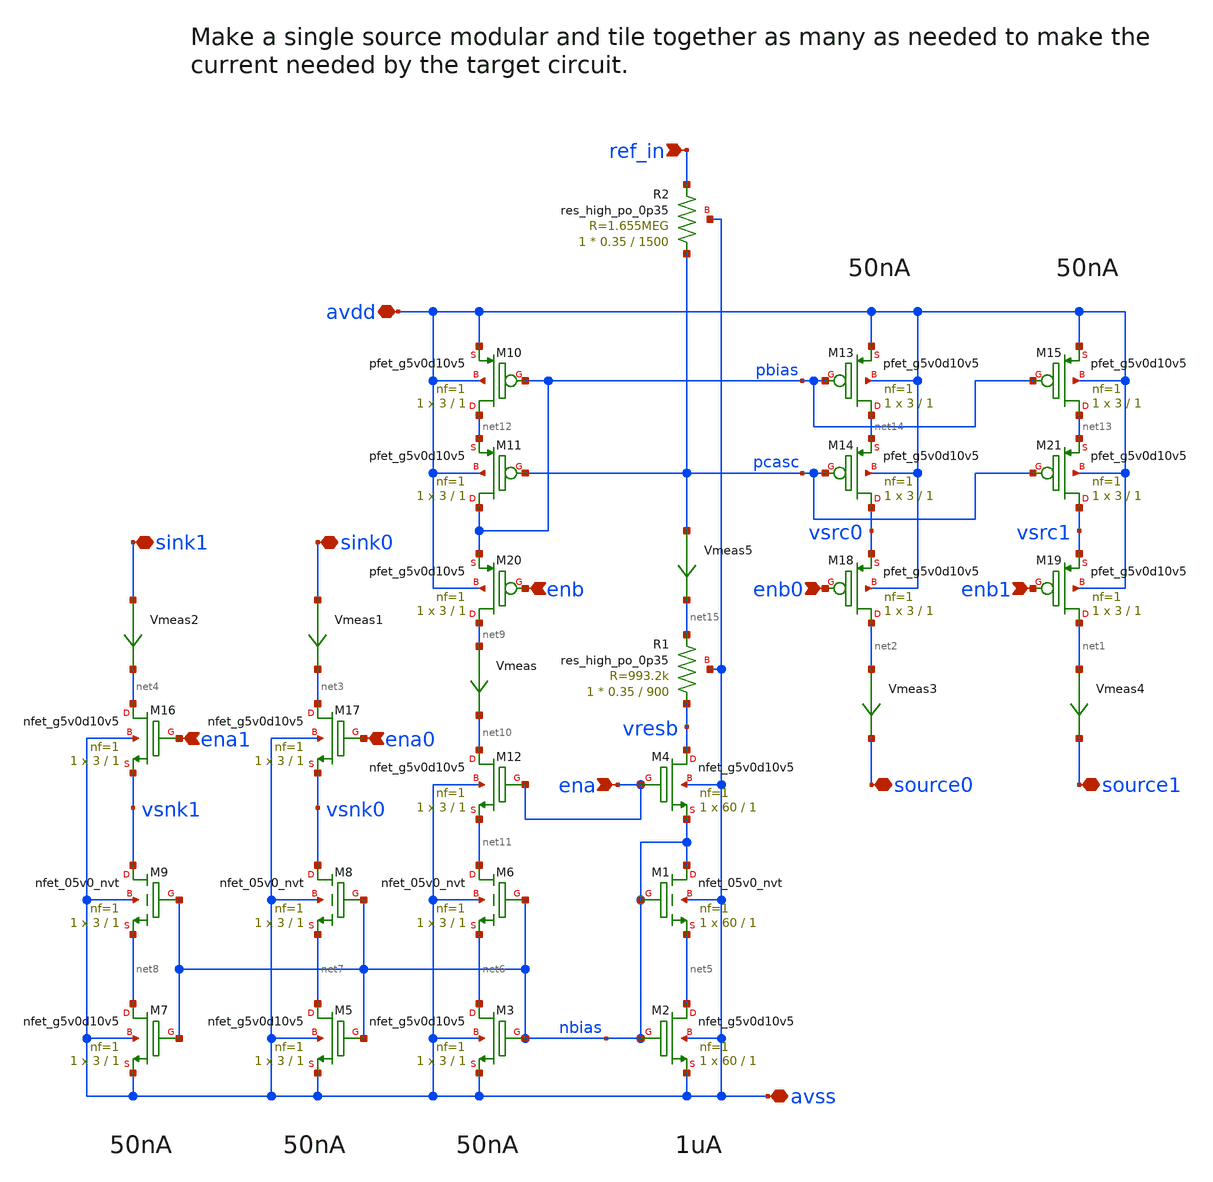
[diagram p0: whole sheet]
** sch_path: xschem/bias_generator_test.sch
**.subckt bias_generator_test ref_in sink0 sink1 avss ena avdd source1 source0 ena0 ena1 enb enb0
*+ enb1
*.ipin ref_in
*.iopin sink0
*.iopin sink1
*.iopin avss
*.ipin ena
*.iopin avdd
*.iopin source1
*.iopin source0
*.ipin ena0
*.ipin ena1
*.ipin enb
*.ipin enb0
*.ipin enb1
XR1 vresb net15 avss sky130_fd_pr__res_high_po_0p35 L=900 mult=1 m=1
XM2 net5 nbias avss avss sky130_fd_pr__nfet_g5v0d10v5 L=1 W=60 nf=1 ad='int((nf+1)/2) * W/nf * 0.29'
+ as='int((nf+2)/2) * W/nf * 0.29' pd='2*int((nf+1)/2) * (W/nf + 0.29)' ps='2*int((nf+2)/2) * (W/nf + 0.29)'
+ nrd='0.29 / W' nrs='0.29 / W' sa=0 sb=0 sd=0 mult=1 m=1
XM3 net6 nbias avss avss sky130_fd_pr__nfet_g5v0d10v5 L=1 W=3 nf=1 ad='int((nf+1)/2) * W/nf * 0.29' as='int((nf+2)/2) * W/nf * 0.29'
+ pd='2*int((nf+1)/2) * (W/nf + 0.29)' ps='2*int((nf+2)/2) * (W/nf + 0.29)' nrd='0.29 / W' nrs='0.29 / W'
+ sa=0 sb=0 sd=0 mult=1 m=1
XM5 net7 nbias avss avss sky130_fd_pr__nfet_g5v0d10v5 L=1 W=3 nf=1 ad='int((nf+1)/2) * W/nf * 0.29' as='int((nf+2)/2) * W/nf * 0.29'
+ pd='2*int((nf+1)/2) * (W/nf + 0.29)' ps='2*int((nf+2)/2) * (W/nf + 0.29)' nrd='0.29 / W' nrs='0.29 / W'
+ sa=0 sb=0 sd=0 mult=1 m=1
XM7 net8 nbias avss avss sky130_fd_pr__nfet_g5v0d10v5 L=1 W=3 nf=1 ad='int((nf+1)/2) * W/nf * 0.29' as='int((nf+2)/2) * W/nf * 0.29'
+ pd='2*int((nf+1)/2) * (W/nf + 0.29)' ps='2*int((nf+2)/2) * (W/nf + 0.29)' nrd='0.29 / W' nrs='0.29 / W'
+ sa=0 sb=0 sd=0 mult=1 m=1
XM10 net12 pbias avdd avdd sky130_fd_pr__pfet_g5v0d10v5 L=1 W=3 nf=1 ad='int((nf+1)/2) * W/nf * 0.29'
+ as='int((nf+2)/2) * W/nf * 0.29' pd='2*int((nf+1)/2) * (W/nf + 0.29)' ps='2*int((nf+2)/2) * (W/nf + 0.29)'
+ nrd='0.29 / W' nrs='0.29 / W' sa=0 sb=0 sd=0 mult=1 m=1
XM13 net14 pbias avdd avdd sky130_fd_pr__pfet_g5v0d10v5 L=1 W=3 nf=1 ad='int((nf+1)/2) * W/nf * 0.29'
+ as='int((nf+2)/2) * W/nf * 0.29' pd='2*int((nf+1)/2) * (W/nf + 0.29)' ps='2*int((nf+2)/2) * (W/nf + 0.29)'
+ nrd='0.29 / W' nrs='0.29 / W' sa=0 sb=0 sd=0 mult=1 m=1
XM15 net13 pbias avdd avdd sky130_fd_pr__pfet_g5v0d10v5 L=1 W=3 nf=1 ad='int((nf+1)/2) * W/nf * 0.29'
+ as='int((nf+2)/2) * W/nf * 0.29' pd='2*int((nf+1)/2) * (W/nf + 0.29)' ps='2*int((nf+2)/2) * (W/nf + 0.29)'
+ nrd='0.29 / W' nrs='0.29 / W' sa=0 sb=0 sd=0 mult=1 m=1
XM18 net2 enb0 vsrc0 avdd sky130_fd_pr__pfet_g5v0d10v5 L=1 W=3 nf=1 ad='int((nf+1)/2) * W/nf * 0.29'
+ as='int((nf+2)/2) * W/nf * 0.29' pd='2*int((nf+1)/2) * (W/nf + 0.29)' ps='2*int((nf+2)/2) * (W/nf + 0.29)'
+ nrd='0.29 / W' nrs='0.29 / W' sa=0 sb=0 sd=0 mult=1 m=1
XM19 net1 enb1 vsrc1 avdd sky130_fd_pr__pfet_g5v0d10v5 L=1 W=3 nf=1 ad='int((nf+1)/2) * W/nf * 0.29'
+ as='int((nf+2)/2) * W/nf * 0.29' pd='2*int((nf+1)/2) * (W/nf + 0.29)' ps='2*int((nf+2)/2) * (W/nf + 0.29)'
+ nrd='0.29 / W' nrs='0.29 / W' sa=0 sb=0 sd=0 mult=1 m=1
XM20 net9 enb pbias avdd sky130_fd_pr__pfet_g5v0d10v5 L=1 W=3 nf=1 ad='int((nf+1)/2) * W/nf * 0.29' as='int((nf+2)/2) * W/nf * 0.29'
+ pd='2*int((nf+1)/2) * (W/nf + 0.29)' ps='2*int((nf+2)/2) * (W/nf + 0.29)' nrd='0.29 / W' nrs='0.29 / W'
+ sa=0 sb=0 sd=0 mult=1 m=1
Vmeas net9 net10 0
.save i(vmeas)
Vmeas1 sink0 net3 0
.save i(vmeas1)
Vmeas2 sink1 net4 0
.save i(vmeas2)
Vmeas3 net2 source0 0
.save i(vmeas3)
Vmeas4 net1 source1 0
.save i(vmeas4)
Vmeas5 pcasc net15 0
.save i(vmeas5)
XM4 vresb ena nbias avss sky130_fd_pr__nfet_g5v0d10v5 L=1 W=60 nf=1 ad='int((nf+1)/2) * W/nf * 0.29'
+ as='int((nf+2)/2) * W/nf * 0.29' pd='2*int((nf+1)/2) * (W/nf + 0.29)' ps='2*int((nf+2)/2) * (W/nf + 0.29)'
+ nrd='0.29 / W' nrs='0.29 / W' sa=0 sb=0 sd=0 mult=1 m=1
XM16 net4 ena1 vsnk1 avss sky130_fd_pr__nfet_g5v0d10v5 L=1 W=3 nf=1 ad='int((nf+1)/2) * W/nf * 0.29'
+ as='int((nf+2)/2) * W/nf * 0.29' pd='2*int((nf+1)/2) * (W/nf + 0.29)' ps='2*int((nf+2)/2) * (W/nf + 0.29)'
+ nrd='0.29 / W' nrs='0.29 / W' sa=0 sb=0 sd=0 mult=1 m=1
XM17 net3 ena0 vsnk0 avss sky130_fd_pr__nfet_g5v0d10v5 L=1 W=3 nf=1 ad='int((nf+1)/2) * W/nf * 0.29'
+ as='int((nf+2)/2) * W/nf * 0.29' pd='2*int((nf+1)/2) * (W/nf + 0.29)' ps='2*int((nf+2)/2) * (W/nf + 0.29)'
+ nrd='0.29 / W' nrs='0.29 / W' sa=0 sb=0 sd=0 mult=1 m=1
XM1 nbias nbias net5 avss sky130_fd_pr__nfet_05v0_nvt L=1 W=60 nf=1 ad='int((nf+1)/2) * W/nf * 0.29'
+ as='int((nf+2)/2) * W/nf * 0.29' pd='2*int((nf+1)/2) * (W/nf + 0.29)' ps='2*int((nf+2)/2) * (W/nf + 0.29)'
+ nrd='0.29 / W' nrs='0.29 / W' sa=0 sb=0 sd=0 mult=1 m=1
XM6 net11 nbias net6 avss sky130_fd_pr__nfet_05v0_nvt L=1 W=3 nf=1 ad='int((nf+1)/2) * W/nf * 0.29' as='int((nf+2)/2) * W/nf * 0.29'
+ pd='2*int((nf+1)/2) * (W/nf + 0.29)' ps='2*int((nf+2)/2) * (W/nf + 0.29)' nrd='0.29 / W' nrs='0.29 / W'
+ sa=0 sb=0 sd=0 mult=1 m=1
XM8 vsnk0 nbias net7 avss sky130_fd_pr__nfet_05v0_nvt L=1 W=3 nf=1 ad='int((nf+1)/2) * W/nf * 0.29' as='int((nf+2)/2) * W/nf * 0.29'
+ pd='2*int((nf+1)/2) * (W/nf + 0.29)' ps='2*int((nf+2)/2) * (W/nf + 0.29)' nrd='0.29 / W' nrs='0.29 / W'
+ sa=0 sb=0 sd=0 mult=1 m=1
XM9 vsnk1 nbias net8 avss sky130_fd_pr__nfet_05v0_nvt L=1 W=3 nf=1 ad='int((nf+1)/2) * W/nf * 0.29' as='int((nf+2)/2) * W/nf * 0.29'
+ pd='2*int((nf+1)/2) * (W/nf + 0.29)' ps='2*int((nf+2)/2) * (W/nf + 0.29)' nrd='0.29 / W' nrs='0.29 / W'
+ sa=0 sb=0 sd=0 mult=1 m=1
XM12 net10 ena net11 avss sky130_fd_pr__nfet_g5v0d10v5 L=1 W=3 nf=1 ad='int((nf+1)/2) * W/nf * 0.29'
+ as='int((nf+2)/2) * W/nf * 0.29' pd='2*int((nf+1)/2) * (W/nf + 0.29)' ps='2*int((nf+2)/2) * (W/nf + 0.29)'
+ nrd='0.29 / W' nrs='0.29 / W' sa=0 sb=0 sd=0 mult=1 m=1
XM11 pbias pcasc net12 avdd sky130_fd_pr__pfet_g5v0d10v5 L=1 W=3 nf=1 ad='int((nf+1)/2) * W/nf * 0.29'
+ as='int((nf+2)/2) * W/nf * 0.29' pd='2*int((nf+1)/2) * (W/nf + 0.29)' ps='2*int((nf+2)/2) * (W/nf + 0.29)'
+ nrd='0.29 / W' nrs='0.29 / W' sa=0 sb=0 sd=0 mult=1 m=1
XM14 vsrc0 pcasc net14 avdd sky130_fd_pr__pfet_g5v0d10v5 L=1 W=3 nf=1 ad='int((nf+1)/2) * W/nf * 0.29'
+ as='int((nf+2)/2) * W/nf * 0.29' pd='2*int((nf+1)/2) * (W/nf + 0.29)' ps='2*int((nf+2)/2) * (W/nf + 0.29)'
+ nrd='0.29 / W' nrs='0.29 / W' sa=0 sb=0 sd=0 mult=1 m=1
XM21 vsrc1 pcasc net13 avdd sky130_fd_pr__pfet_g5v0d10v5 L=1 W=3 nf=1 ad='int((nf+1)/2) * W/nf * 0.29'
+ as='int((nf+2)/2) * W/nf * 0.29' pd='2*int((nf+1)/2) * (W/nf + 0.29)' ps='2*int((nf+2)/2) * (W/nf + 0.29)'
+ nrd='0.29 / W' nrs='0.29 / W' sa=0 sb=0 sd=0 mult=1 m=1
XR2 pcasc ref_in avss sky130_fd_pr__res_high_po_0p35 L=1500 mult=1 m=1
**.ends
.end
